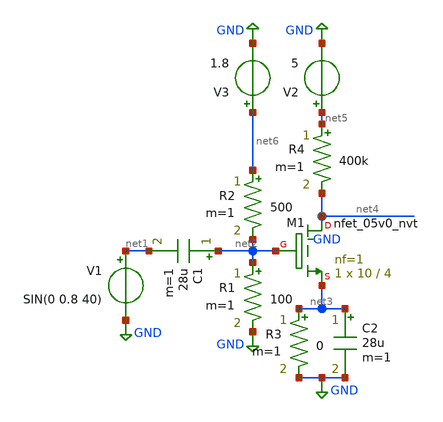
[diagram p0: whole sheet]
** sch_path: xschem/cs3v3-abstract.sch
**.subckt cs3v3-abstract
V1 net1 GND SIN(0 0.8 40)
C1 net2 net1 28u m=1
R1 net2 GND 100 m=1
R2 net6 net2 500 m=1
R3 net3 GND 0 m=1
C2 net3 GND 28u m=1
R4 net5 net4 400k m=1
V2 net5 GND 5
V3 net6 GND 1.8
XM1 net4 net2 net3 GND sky130_fd_pr__nfet_05v0_nvt L=4 W=10 nf=1 ad='int((nf+1)/2) * W/nf * 0.29' as='int((nf+2)/2) * W/nf * 0.29'
+ pd='2*int((nf+1)/2) * (W/nf + 0.29)' ps='2*int((nf+2)/2) * (W/nf + 0.29)' nrd='0.29 / W' nrs='0.29 / W'
+ sa=0 sb=0 sd=0 mult=1 m=1
**** begin user architecture code
 ** manual skywater pdks install (with patches applied)
* .lib $::SKYWATER_MODELS/models/sky130.lib.spice tt

** opencircuitdesign pdks install
.lib $::SKYWATER_MODELS/sky130.lib.spice tt

.param mc_mm_switch=0
.param mc_pr_switch=0



.tran 0.001s 0.1s
.control
  run
  plot v(net4) v(net2)
.endc
.save all


**** end user architecture code
**.ends
.GLOBAL GND
.end
